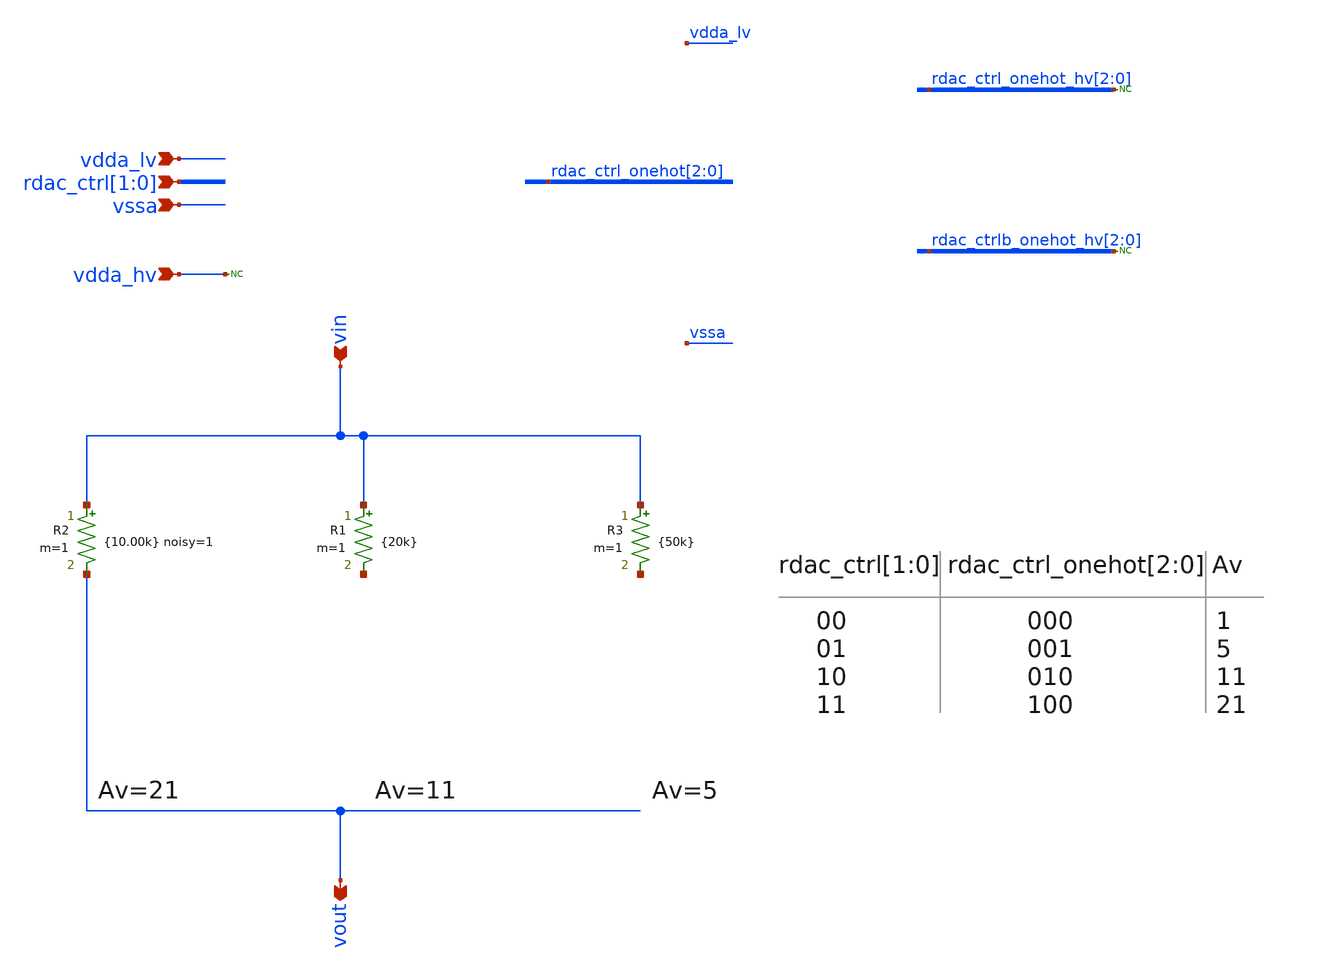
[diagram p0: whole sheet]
** sch_path: Design_Review_1/Testbench_2_tb_sunrise_ina_idealR_NOISE/rdac_no_sws_av21.sch
**.subckt rdac_no_sws_av21 vin vout vdda_lv vssa rdac_ctrl[1],rdac_ctrl[0] vdda_hv
*.ipin vin
*.opin vout
*.ipin vdda_lv
*.ipin vssa
*.ipin rdac_ctrl[1],rdac_ctrl[0]
*.ipin vdda_hv
R2 vin vout {10.00k} noisy=1 m=1
R1 vin net1 {20k} m=1
R3 vin net2 {50k} m=1
* noconn vdda_hv
* noconn rdac_ctrl_onehot_hv[2:0]
* noconn rdac_ctrlb_onehot_hv[2:0]
**.ends
.end
